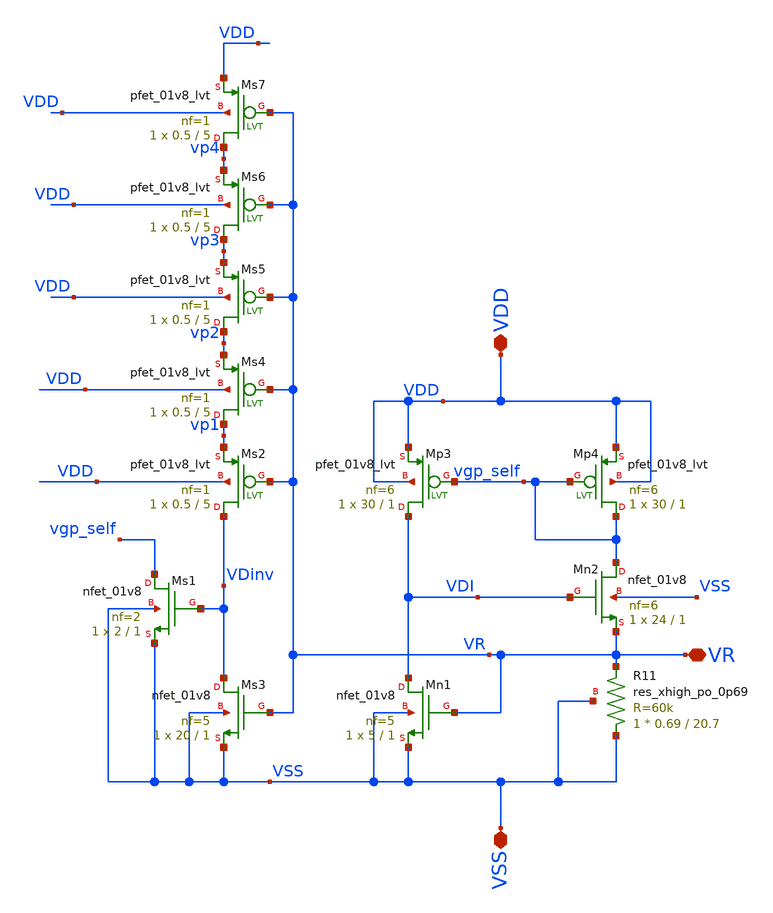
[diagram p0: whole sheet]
** sch_path: xschem/Iref/self_bias.sch
**.subckt self_bias VR VDD VSS
*.iopin VR
*.iopin VDD
*.iopin VSS
XMp4 vgp_self vgp_self VDD VDD sky130_fd_pr__pfet_01v8_lvt L=1 W=30 nf=6 ad='int((6 + 1)/2) * 30 / 6 * 0.29'
+ as='int((6 + 2)/2) * 30 / 6 * 0.29' pd='2*int((6 + 1)/2) * (30 / 6 + 0.29)' ps='2*int((6 + 2)/2) * (30 / 6 + 0.29)'
+ nrd='0.29 / 30 ' nrs='0.29 / 30 ' sa=0 sb=0 sd=0 mult=1 m=1
XMp3 VDI vgp_self VDD VDD sky130_fd_pr__pfet_01v8_lvt L=1 W=30 nf=6 ad='int((6 + 1)/2) * 30 / 6 * 0.29'
+ as='int((6 + 2)/2) * 30 / 6 * 0.29' pd='2*int((6 + 1)/2) * (30 / 6 + 0.29)' ps='2*int((6 + 2)/2) * (30 / 6 + 0.29)'
+ nrd='0.29 / 30 ' nrs='0.29 / 30 ' sa=0 sb=0 sd=0 mult=1 m=1
XMs2 VDinv VR vp1 VDD sky130_fd_pr__pfet_01v8_lvt L=5 W=0.5 nf=1 ad='int((1 + 1)/2) * 0.5 / 1 * 0.29'
+ as='int((1 + 2)/2) * 0.5 / 1 * 0.29' pd='2*int((1 + 1)/2) * (0.5 / 1 + 0.29)' ps='2*int((1 + 2)/2) * (0.5 / 1 + 0.29)'
+ nrd='0.29 / 0.5 ' nrs='0.29 / 0.5 ' sa=0 sb=0 sd=0 mult=1 m=1
XMn2 vgp_self VDI VR VSS sky130_fd_pr__nfet_01v8 L=1 W=24 nf=6 ad='int((6 + 1)/2) * 24 / 6 * 0.29' as='int((6 + 2)/2) * 24 / 6 * 0.29'
+ pd='2*int((6 + 1)/2) * (24 / 6 + 0.29)' ps='2*int((6 + 2)/2) * (24 / 6 + 0.29)' nrd='0.29 / 24 ' nrs='0.29 / 24 '
+ sa=0 sb=0 sd=0 mult=1 m=1
XMn1 VDI VR VSS VSS sky130_fd_pr__nfet_01v8 L=1 W=5 nf=5 ad='int((5 + 1)/2) * 5 / 5 * 0.29' as='int((5 + 2)/2) * 5 / 5 * 0.29'
+ pd='2*int((5 + 1)/2) * (5 / 5 + 0.29)' ps='2*int((5 + 2)/2) * (5 / 5 + 0.29)' nrd='0.29 / 5 ' nrs='0.29 / 5 '
+ sa=0 sb=0 sd=0 mult=1 m=1
XMs3 VDinv VR VSS VSS sky130_fd_pr__nfet_01v8 L=1 W=20 nf=5 ad='int((5 + 1)/2) * 20 / 5 * 0.29' as='int((5 + 2)/2) * 20 / 5 * 0.29'
+ pd='2*int((5 + 1)/2) * (20 / 5 + 0.29)' ps='2*int((5 + 2)/2) * (20 / 5 + 0.29)' nrd='0.29 / 20 ' nrs='0.29 / 20 '
+ sa=0 sb=0 sd=0 mult=1 m=1
XMs1 vgp_self VDinv VSS VSS sky130_fd_pr__nfet_01v8 L=1 W=2 nf=2 ad='int((2 + 1)/2) * 2 / 2 * 0.29' as='int((2 + 2)/2) * 2 / 2 * 0.29'
+ pd='2*int((2 + 1)/2) * (2 / 2 + 0.29)' ps='2*int((2 + 2)/2) * (2 / 2 + 0.29)' nrd='0.29 / 2 ' nrs='0.29 / 2 '
+ sa=0 sb=0 sd=0 mult=1 m=1
XR11 VSS VR VSS sky130_fd_pr__res_xhigh_po_0p69 L=20.7 mult=1 m=1
XMs4 vp1 VR vp2 VDD sky130_fd_pr__pfet_01v8_lvt L=5 W=0.5 nf=1 ad='int((1 + 1)/2) * 0.5 / 1 * 0.29' as='int((1 + 2)/2) * 0.5 / 1 * 0.29'
+ pd='2*int((1 + 1)/2) * (0.5 / 1 + 0.29)' ps='2*int((1 + 2)/2) * (0.5 / 1 + 0.29)' nrd='0.29 / 0.5 ' nrs='0.29 / 0.5 '
+ sa=0 sb=0 sd=0 mult=1 m=1
XMs5 vp2 VR vp3 VDD sky130_fd_pr__pfet_01v8_lvt L=5 W=0.5 nf=1 ad='int((1 + 1)/2) * 0.5 / 1 * 0.29' as='int((1 + 2)/2) * 0.5 / 1 * 0.29'
+ pd='2*int((1 + 1)/2) * (0.5 / 1 + 0.29)' ps='2*int((1 + 2)/2) * (0.5 / 1 + 0.29)' nrd='0.29 / 0.5 ' nrs='0.29 / 0.5 '
+ sa=0 sb=0 sd=0 mult=1 m=1
XMs6 vp3 VR vp4 VDD sky130_fd_pr__pfet_01v8_lvt L=5 W=0.5 nf=1 ad='int((1 + 1)/2) * 0.5 / 1 * 0.29' as='int((1 + 2)/2) * 0.5 / 1 * 0.29'
+ pd='2*int((1 + 1)/2) * (0.5 / 1 + 0.29)' ps='2*int((1 + 2)/2) * (0.5 / 1 + 0.29)' nrd='0.29 / 0.5 ' nrs='0.29 / 0.5 '
+ sa=0 sb=0 sd=0 mult=1 m=1
XMs7 vp4 VR VDD VDD sky130_fd_pr__pfet_01v8_lvt L=5 W=0.5 nf=1 ad='int((1 + 1)/2) * 0.5 / 1 * 0.29' as='int((1 + 2)/2) * 0.5 / 1 * 0.29'
+ pd='2*int((1 + 1)/2) * (0.5 / 1 + 0.29)' ps='2*int((1 + 2)/2) * (0.5 / 1 + 0.29)' nrd='0.29 / 0.5 ' nrs='0.29 / 0.5 '
+ sa=0 sb=0 sd=0 mult=1 m=1
**.ends
.end
